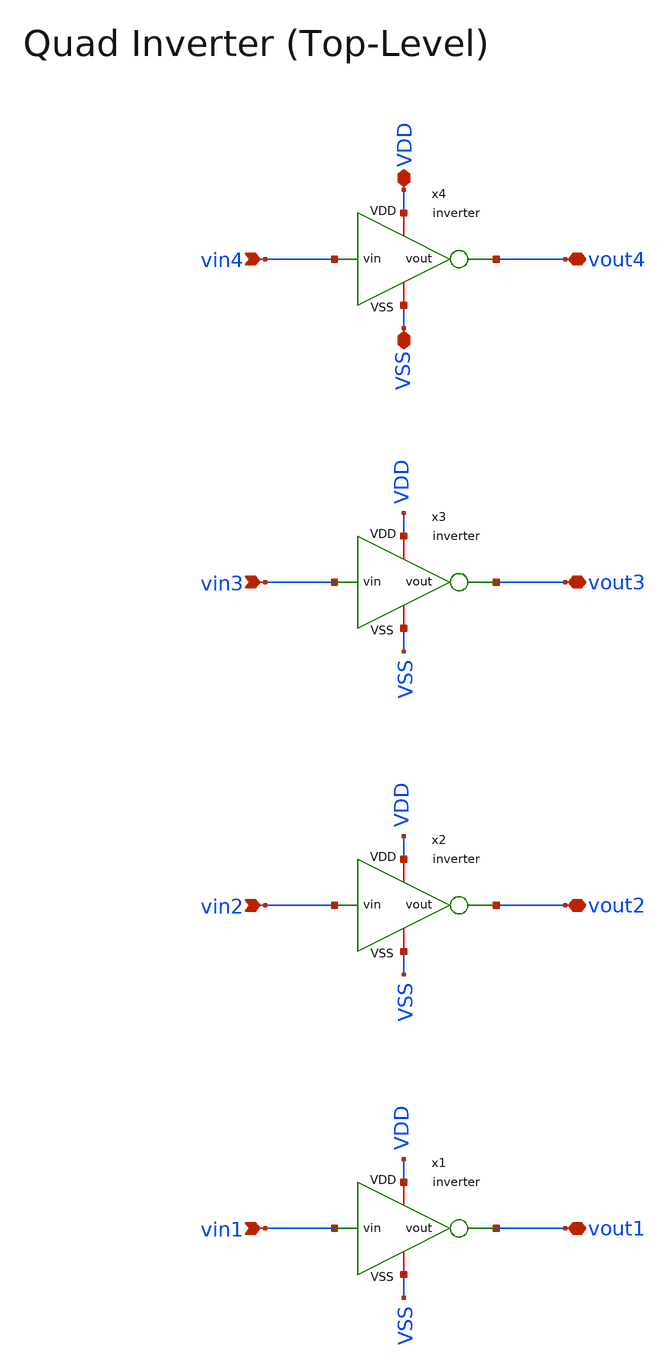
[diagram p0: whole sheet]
** sch_path: macros/inverter/schematic/xschem/inverter_top.sch
**.subckt inverter_top vin4 VDD VSS vout4 vin3 vin2 vin1 vout3 vout2 vout1
*.ipin vin4
*.iopin VDD
*.iopin VSS
*.iopin vout4
*.ipin vin3
*.ipin vin2
*.ipin vin1
*.iopin vout3
*.iopin vout2
*.iopin vout1
x1 VDD vin1 vout1 VSS inverter
x2 VDD vin2 vout2 VSS inverter
x3 VDD vin3 vout3 VSS inverter
x4 VDD vin4 vout4 VSS inverter
**.ends
.end
